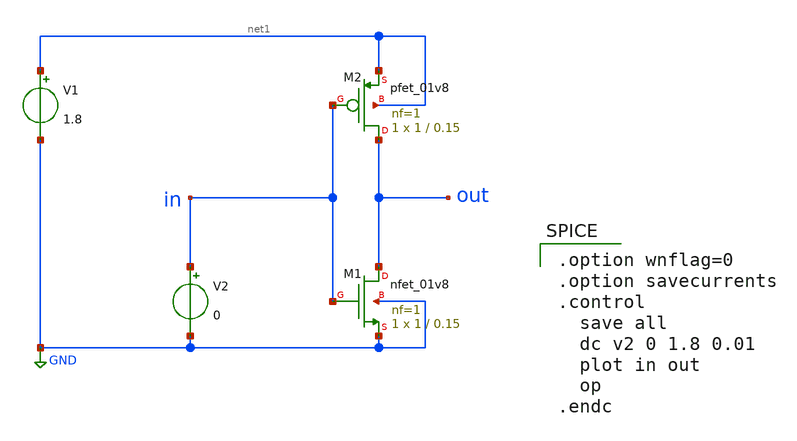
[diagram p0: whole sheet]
** sch_path: cmos_inverter.sch
**.subckt cmos_inverter
XM1 out in GND GND sky130_fd_pr__nfet_01v8 L=0.15 W=1 nf=1 ad='int((1 + 1)/2) * 1 / 1 * 0.29' as='int((1 + 2)/2) * 1 / 1 * 0.29'
+ pd='2*int((1 + 1)/2) * (1 / 1 + 0.29)' ps='2*int((1 + 2)/2) * (1 / 1 + 0.29)' nrd='0.29 / 1 ' nrs='0.29 / 1 '
+ sa=0 sb=0 sd=0 mult=1 m=1
XM2 out in net1 net1 sky130_fd_pr__pfet_01v8 L=0.15 W=1 nf=1 ad='int((1 + 1)/2) * 1 / 1 * 0.29' as='int((1 + 2)/2) * 1 / 1 * 0.29'
+ pd='2*int((1 + 1)/2) * (1 / 1 + 0.29)' ps='2*int((1 + 2)/2) * (1 / 1 + 0.29)' nrd='0.29 / 1 ' nrs='0.29 / 1 '
+ sa=0 sb=0 sd=0 mult=1 m=1
V1 net1 GND 1.8
V2 in GND 0
**** begin user architecture code
 .lib /foss/pdks/ciel/sky130/versions/7b70722e33c03fcb5dabcf4d479fb0822d9251c9/sky130A/libs.tech/ngspice/sky130.lib.spice tt
.param mc_mm_switch=0
.param mc_pr_switch=1

.option wnflag=0
.option savecurrents
.control
  save all
  dc v2 0 1.8 0.01
  plot in out
  op
.endc

**** end user architecture code
**.ends
.GLOBAL GND
.end
